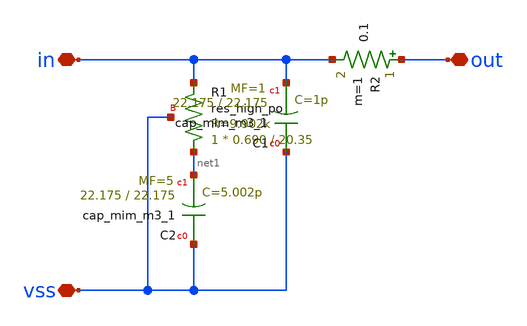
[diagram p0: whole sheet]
** sch_path: custom_gds/tt_um_mickey_pll/xschem/lpf.sch
**.subckt lpf in vss out
*.iopin in
*.iopin vss
*.iopin out
R2 out in 0.1 m=1
XR1 net1 in vss sky130_fd_pr__res_high_po W=0.690 L=20.35 mult=1 m=1
XC1 vss in sky130_fd_pr__cap_mim_m3_1 W=22.175 L=22.175 MF=1 m=1
XC2 vss net1 sky130_fd_pr__cap_mim_m3_1 W=22.175 L=22.175 MF=5 m=5
**.ends
.end
